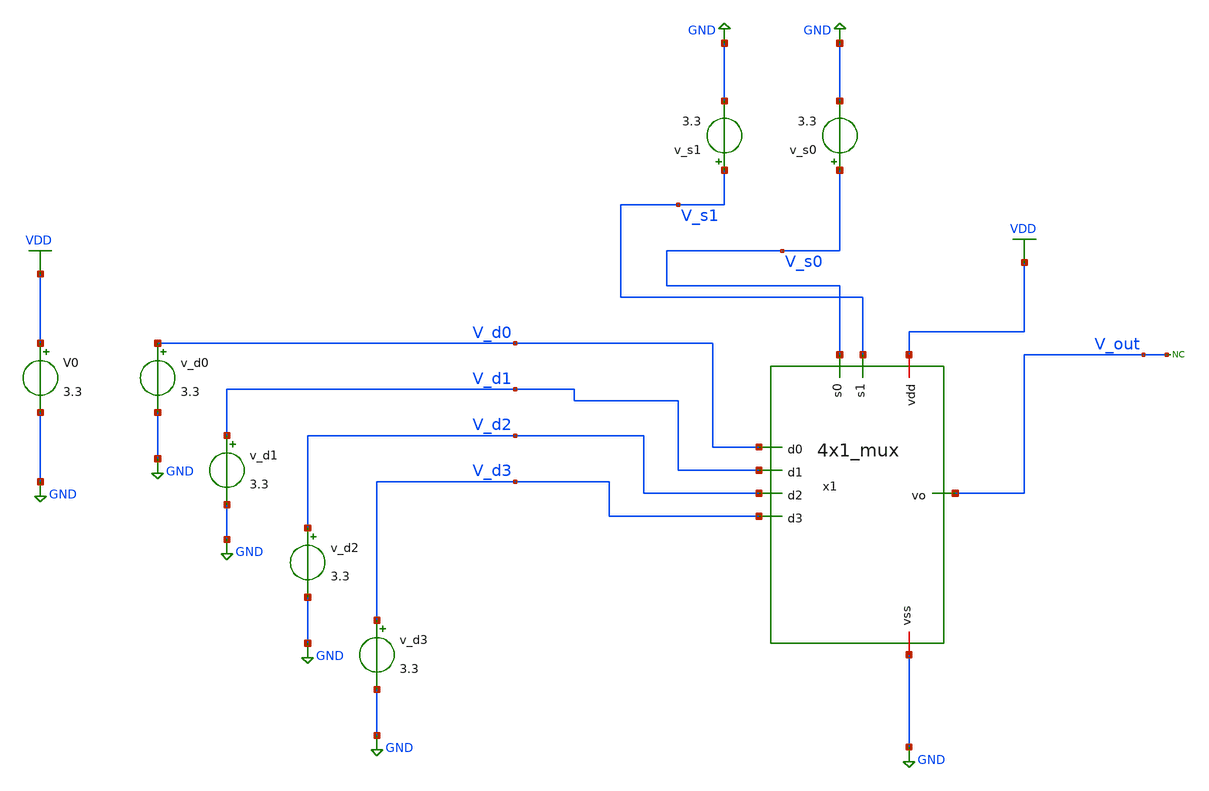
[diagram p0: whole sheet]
** sch_path: designs/4x1_mux_tb.sch
**.subckt 4x1_mux_tb
x1 V_s1 V_s0 VDD V_d0 V_d1 V_out V_d2 V_d3 GND 4x1_mux
v_d0 V_d0 GND 3.3
v_d1 V_d1 GND 3.3
v_d2 V_d2 GND 3.3
v_d3 V_d3 GND 3.3
v_s0 V_s0 GND 3.3
v_s1 V_s1 GND 3.3
V0 VDD GND 3.3
* noconn V_out
**** begin user architecture code


.control
save all

* Define transient params to test all 4 select states
let t_base = 80n
* Run for 160ns to see all 4 select states
let tstop = 2 * t_base
let tstep = t_base / 2000

* Override schematic DC sources with PULSE definitions for SELECT lines
alter @v_s0[PULSE] = [ 0 3.3 0 100p 100p 39.9n 80n ]
alter @v_s1[PULSE] = [ 0 3.3 0 100p 100p 79.9n 160n ]

* Set static DC values for DATA lines
alter @v_d0[DC] = 3.3
alter @v_d1[DC] = 0
alter @v_d2[DC] = 3.3
alter @v_d3[DC] = 0

* Simulations
op
tran $&tstep $&tstop

* Plots
setplot tran1
let s0 = v(V_s0)
let s1 = v(V_s1)
let vout = v(V_out)
* Data lines for reference if needed
let d0 = v(V_d0)

plot v(V_out) v(V_s0)+4 v(V_s1)+8 title 4x1


.include $::180MCU_MODELS/design.ngspice
.lib $::180MCU_MODELS/sm141064.ngspice typical

**** end user architecture code
**.ends

* expanding   symbol:  4x1_mux.sym # of pins=9
** sym_path: designs/4x1_mux.sym
** sch_path: designs/4x1_mux.sch
.subckt 4x1_mux s1 s0 vdd d0 d1 vo d2 d3 vss
*.ipin d0
*.ipin d1
*.ipin d2
*.ipin d3
*.ipin s1
*.ipin s0
*.iopin vdd
*.iopin vss
*.opin vo
x1 net7 s1 net1 net8 inv
x2 net9 s0 net2 net10 inv
x3 vdd net6 d0 net1 net2 vss 3_input_and
x4 vdd net5 d1 net1 s0 vss 3_input_and
x5 vdd net4 d2 s1 net2 vss 3_input_and
x6 vdd net3 d3 s1 s0 vss 3_input_and
x7 net11 net6 net5 net4 net3 vo net12 4_input_or
.ends


* expanding   symbol:  inv.sym # of pins=4
** sym_path: designs/inv.sym
** sch_path: designs/inv.sch
.subckt inv vdd vin vout vss
*.iopin vdd
*.iopin vss
*.ipin vin
*.opin vout
XM1 vout vin vdd vdd pfet_03v3 L=0.28u W=0.22u nf=1 ad='int((nf+1)/2) * W/nf * 0.18u' as='int((nf+2)/2) * W/nf * 0.18u'
+ pd='2*int((nf+1)/2) * (W/nf + 0.18u)' ps='2*int((nf+2)/2) * (W/nf + 0.18u)' nrd='0.18u / W' nrs='0.18u / W'
+ sa=0 sb=0 sd=0 m=1
XM2 vout vin vss vss nfet_03v3 L=0.28u W=0.22u nf=1 ad='int((nf+1)/2) * W/nf * 0.18u' as='int((nf+2)/2) * W/nf * 0.18u'
+ pd='2*int((nf+1)/2) * (W/nf + 0.18u)' ps='2*int((nf+2)/2) * (W/nf + 0.18u)' nrd='0.18u / W' nrs='0.18u / W'
+ sa=0 sb=0 sd=0 m=1
.ends


* expanding   symbol:  3_input_and.sym # of pins=6
** sym_path: designs/3_input_and.sym
** sch_path: designs/3_input_and.sch
.subckt 3_input_and vdd Vo Vi_1 Vi_2 Vi_3 vss
*.iopin vdd
*.iopin vss
*.ipin Vi_1
*.ipin Vi_2
*.ipin Vi_3
*.opin Vo
XM1 net1 Vi_1 vdd vdd pfet_03v3 L=0.28u W=0.22u nf=1 ad='int((nf+1)/2) * W/nf * 0.18u' as='int((nf+2)/2) * W/nf * 0.18u'
+ pd='2*int((nf+1)/2) * (W/nf + 0.18u)' ps='2*int((nf+2)/2) * (W/nf + 0.18u)' nrd='0.18u / W' nrs='0.18u / W'
+ sa=0 sb=0 sd=0 m=1
XM2 net1 Vi_2 vdd vdd pfet_03v3 L=0.28u W=0.22u nf=1 ad='int((nf+1)/2) * W/nf * 0.18u' as='int((nf+2)/2) * W/nf * 0.18u'
+ pd='2*int((nf+1)/2) * (W/nf + 0.18u)' ps='2*int((nf+2)/2) * (W/nf + 0.18u)' nrd='0.18u / W' nrs='0.18u / W'
+ sa=0 sb=0 sd=0 m=1
XM3 net1 Vi_3 vdd vdd pfet_03v3 L=0.28u W=0.22u nf=1 ad='int((nf+1)/2) * W/nf * 0.18u' as='int((nf+2)/2) * W/nf * 0.18u'
+ pd='2*int((nf+1)/2) * (W/nf + 0.18u)' ps='2*int((nf+2)/2) * (W/nf + 0.18u)' nrd='0.18u / W' nrs='0.18u / W'
+ sa=0 sb=0 sd=0 m=1
XM4 net1 Vi_1 net3 vss nfet_03v3 L=0.28u W=0.22u nf=1 ad='int((nf+1)/2) * W/nf * 0.18u' as='int((nf+2)/2) * W/nf * 0.18u'
+ pd='2*int((nf+1)/2) * (W/nf + 0.18u)' ps='2*int((nf+2)/2) * (W/nf + 0.18u)' nrd='0.18u / W' nrs='0.18u / W'
+ sa=0 sb=0 sd=0 m=1
XM5 net3 Vi_2 net2 vss nfet_03v3 L=0.28u W=0.22u nf=1 ad='int((nf+1)/2) * W/nf * 0.18u' as='int((nf+2)/2) * W/nf * 0.18u'
+ pd='2*int((nf+1)/2) * (W/nf + 0.18u)' ps='2*int((nf+2)/2) * (W/nf + 0.18u)' nrd='0.18u / W' nrs='0.18u / W'
+ sa=0 sb=0 sd=0 m=1
XM6 net2 Vi_3 vss vss nfet_03v3 L=0.28u W=0.22u nf=1 ad='int((nf+1)/2) * W/nf * 0.18u' as='int((nf+2)/2) * W/nf * 0.18u'
+ pd='2*int((nf+1)/2) * (W/nf + 0.18u)' ps='2*int((nf+2)/2) * (W/nf + 0.18u)' nrd='0.18u / W' nrs='0.18u / W'
+ sa=0 sb=0 sd=0 m=1
XM7 Vo net1 vdd vdd pfet_03v3 L=0.28u W=0.22u nf=1 ad='int((nf+1)/2) * W/nf * 0.18u' as='int((nf+2)/2) * W/nf * 0.18u'
+ pd='2*int((nf+1)/2) * (W/nf + 0.18u)' ps='2*int((nf+2)/2) * (W/nf + 0.18u)' nrd='0.18u / W' nrs='0.18u / W'
+ sa=0 sb=0 sd=0 m=1
XM8 Vo net1 vss vss nfet_03v3 L=0.28u W=0.22u nf=1 ad='int((nf+1)/2) * W/nf * 0.18u' as='int((nf+2)/2) * W/nf * 0.18u'
+ pd='2*int((nf+1)/2) * (W/nf + 0.18u)' ps='2*int((nf+2)/2) * (W/nf + 0.18u)' nrd='0.18u / W' nrs='0.18u / W'
+ sa=0 sb=0 sd=0 m=1
.ends


* expanding   symbol:  4_input_or.sym # of pins=7
** sym_path: designs/4_input_or.sym
** sch_path: designs/4_input_or.sch
.subckt 4_input_or vdd vin_0 vin_1 vin_2 vin_3 vout vss
*.iopin vdd
*.iopin vss
*.ipin vin_0
*.ipin vin_1
*.ipin vin_2
*.ipin vin_3
*.opin vout
XM1 net1 vin_0 vdd vdd pfet_03v3 L=0.28u W=0.22u nf=1 ad='int((nf+1)/2) * W/nf * 0.18u' as='int((nf+2)/2) * W/nf * 0.18u'
+ pd='2*int((nf+1)/2) * (W/nf + 0.18u)' ps='2*int((nf+2)/2) * (W/nf + 0.18u)' nrd='0.18u / W' nrs='0.18u / W'
+ sa=0 sb=0 sd=0 m=1
XM2 net4 vin_3 vss vss nfet_03v3 L=0.28u W=0.22u nf=1 ad='int((nf+1)/2) * W/nf * 0.18u' as='int((nf+2)/2) * W/nf * 0.18u'
+ pd='2*int((nf+1)/2) * (W/nf + 0.18u)' ps='2*int((nf+2)/2) * (W/nf + 0.18u)' nrd='0.18u / W' nrs='0.18u / W'
+ sa=0 sb=0 sd=0 m=1
XM3 net2 vin_1 net1 vdd pfet_03v3 L=0.28u W=0.22u nf=1 ad='int((nf+1)/2) * W/nf * 0.18u' as='int((nf+2)/2) * W/nf * 0.18u'
+ pd='2*int((nf+1)/2) * (W/nf + 0.18u)' ps='2*int((nf+2)/2) * (W/nf + 0.18u)' nrd='0.18u / W' nrs='0.18u / W'
+ sa=0 sb=0 sd=0 m=1
XM4 net3 vin_2 net2 vdd pfet_03v3 L=0.28u W=0.22u nf=1 ad='int((nf+1)/2) * W/nf * 0.18u' as='int((nf+2)/2) * W/nf * 0.18u'
+ pd='2*int((nf+1)/2) * (W/nf + 0.18u)' ps='2*int((nf+2)/2) * (W/nf + 0.18u)' nrd='0.18u / W' nrs='0.18u / W'
+ sa=0 sb=0 sd=0 m=1
XM5 net4 vin_3 net3 vdd pfet_03v3 L=0.28u W=0.22u nf=1 ad='int((nf+1)/2) * W/nf * 0.18u' as='int((nf+2)/2) * W/nf * 0.18u'
+ pd='2*int((nf+1)/2) * (W/nf + 0.18u)' ps='2*int((nf+2)/2) * (W/nf + 0.18u)' nrd='0.18u / W' nrs='0.18u / W'
+ sa=0 sb=0 sd=0 m=1
XM6 net4 vin_2 vss vss nfet_03v3 L=0.28u W=0.22u nf=1 ad='int((nf+1)/2) * W/nf * 0.18u' as='int((nf+2)/2) * W/nf * 0.18u'
+ pd='2*int((nf+1)/2) * (W/nf + 0.18u)' ps='2*int((nf+2)/2) * (W/nf + 0.18u)' nrd='0.18u / W' nrs='0.18u / W'
+ sa=0 sb=0 sd=0 m=1
XM7 net4 vin_1 vss vss nfet_03v3 L=0.28u W=0.22u nf=1 ad='int((nf+1)/2) * W/nf * 0.18u' as='int((nf+2)/2) * W/nf * 0.18u'
+ pd='2*int((nf+1)/2) * (W/nf + 0.18u)' ps='2*int((nf+2)/2) * (W/nf + 0.18u)' nrd='0.18u / W' nrs='0.18u / W'
+ sa=0 sb=0 sd=0 m=1
XM8 net4 vin_0 vss vss nfet_03v3 L=0.28u W=0.22u nf=1 ad='int((nf+1)/2) * W/nf * 0.18u' as='int((nf+2)/2) * W/nf * 0.18u'
+ pd='2*int((nf+1)/2) * (W/nf + 0.18u)' ps='2*int((nf+2)/2) * (W/nf + 0.18u)' nrd='0.18u / W' nrs='0.18u / W'
+ sa=0 sb=0 sd=0 m=1
XM9 vout net4 vdd vdd pfet_03v3 L=0.28u W=0.22u nf=1 ad='int((nf+1)/2) * W/nf * 0.18u' as='int((nf+2)/2) * W/nf * 0.18u'
+ pd='2*int((nf+1)/2) * (W/nf + 0.18u)' ps='2*int((nf+2)/2) * (W/nf + 0.18u)' nrd='0.18u / W' nrs='0.18u / W'
+ sa=0 sb=0 sd=0 m=1
XM10 vout net4 vss vss nfet_03v3 L=0.28u W=0.22u nf=1 ad='int((nf+1)/2) * W/nf * 0.18u' as='int((nf+2)/2) * W/nf * 0.18u'
+ pd='2*int((nf+1)/2) * (W/nf + 0.18u)' ps='2*int((nf+2)/2) * (W/nf + 0.18u)' nrd='0.18u / W' nrs='0.18u / W'
+ sa=0 sb=0 sd=0 m=1
.ends

.GLOBAL VDD
.GLOBAL GND
.end
